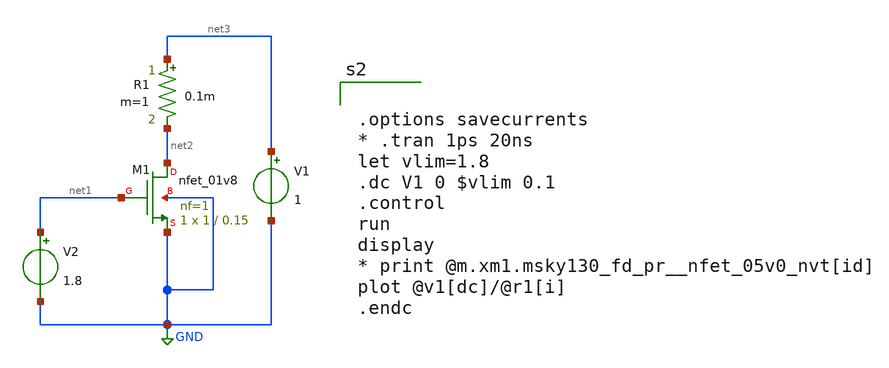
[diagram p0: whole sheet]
** sch_path: xschem/untitled-7.sch
**.subckt untitled-7
V1 net3 GND 1
V2 net1 GND 1.8
R1 net3 net2 0.1m m=1
XM1 net2 net1 GND GND sky130_fd_pr__nfet_01v8 L=0.15 W=1 nf=1 ad='int((nf+1)/2) * W/nf * 0.29' as='int((nf+2)/2) * W/nf * 0.29'
+ pd='2*int((nf+1)/2) * (W/nf + 0.29)' ps='2*int((nf+2)/2) * (W/nf + 0.29)' nrd='0.29 / W' nrs='0.29 / W'
+ sa=0 sb=0 sd=0 mult=1 m=1
**** begin user architecture code
.lib $::SKYWATER_MODELS/sky130.lib.spice ff
* .include $::PDKPATH/libs.ref/sky130_fd_sc_hvl/spice/sky130_fd_sc_hvl.spice



.options savecurrents
* .tran 1ps 20ns
let vlim=1.8
.dc V1 0 $vlim 0.1
.control
run
display
* print @m.xm1.msky130_fd_pr__nfet_05v0_nvt[id]
plot @v1[dc]/@r1[i]
.endc


**** end user architecture code
**.ends
.GLOBAL GND
.end
